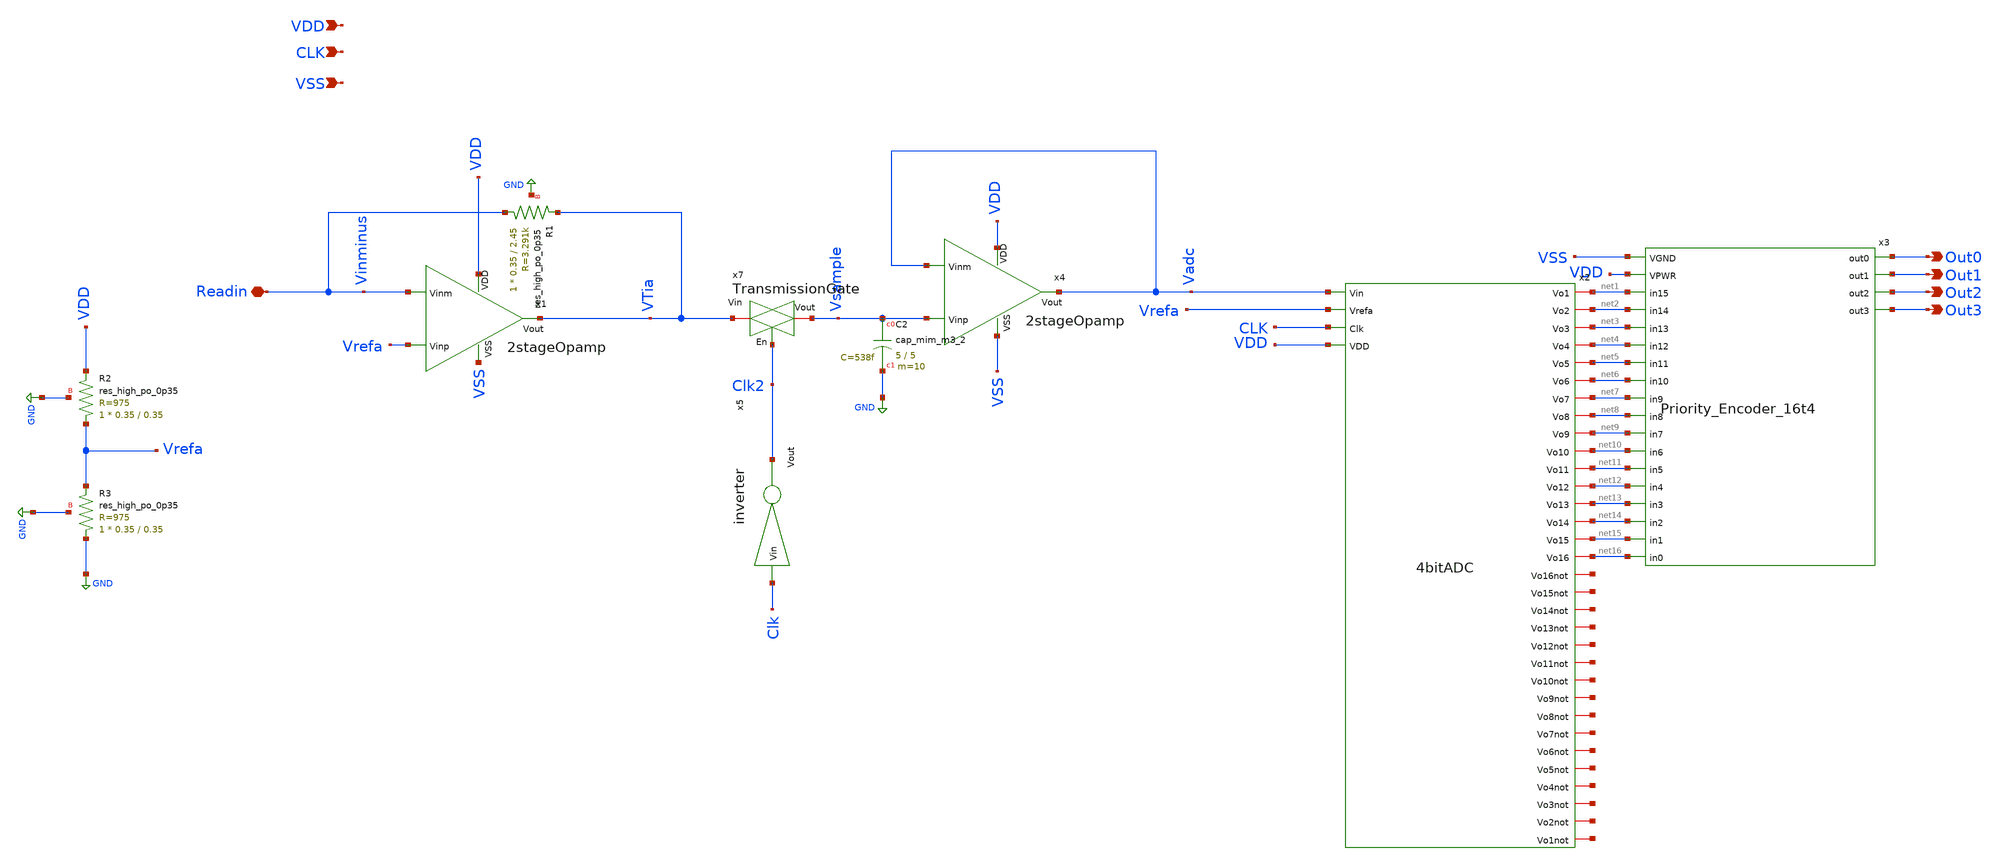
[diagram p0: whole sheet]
** sch_path: Final/PeripheryCircuit.sch
**.subckt PeripheryCircuit Readin Out0 Out1 Out2 Out3 VDD CLK VSS
*.iopin Readin
*.opin Out0
*.opin Out1
*.opin Out2
*.opin Out3
*.ipin VDD
*.ipin CLK
*.ipin VSS
x1 VDD Vinminus Vrefa VTia VSS 2stageOpamp
x2 net1 net2 Vadc net3 Vrefa net4 net5 CLK net6 net7 VDD net8 net9 net10 net11 net12 net13 net14
+ net15 net16 net17 net18 net19 net20 net21 net22 net23 net24 net25 net26 net27 net28 net29 net30 net31
+ net32 4bitADC
x3 VSS VDD net16 net15 net6 net5 net4 net3 net2 net1 net14 net13 net12 net11 net10 net9 net8 net7
+ Out0 Out1 Out2 Out3 Priority_Encoder_16t4
XR1 Vinminus VTia GND sky130_fd_pr__res_high_po_0p35 L=2.45 mult=1 m=1
XR2 Vrefa VDD GND sky130_fd_pr__res_high_po_0p35 L=0.35 mult=1 m=1
XR3 GND Vrefa GND sky130_fd_pr__res_high_po_0p35 L=0.35 mult=1 m=1
x5 Clk2 Clk inverter
x4 VDD Vadc Vsample Vadc VSS 2stageOpamp
x7 VTia Clk2 Vsample TransmissionGate
XC2 Vsample GND sky130_fd_pr__cap_mim_m3_2 W=5 L=5 MF=10 m=10
**.ends
.GLOBAL GND
.end
